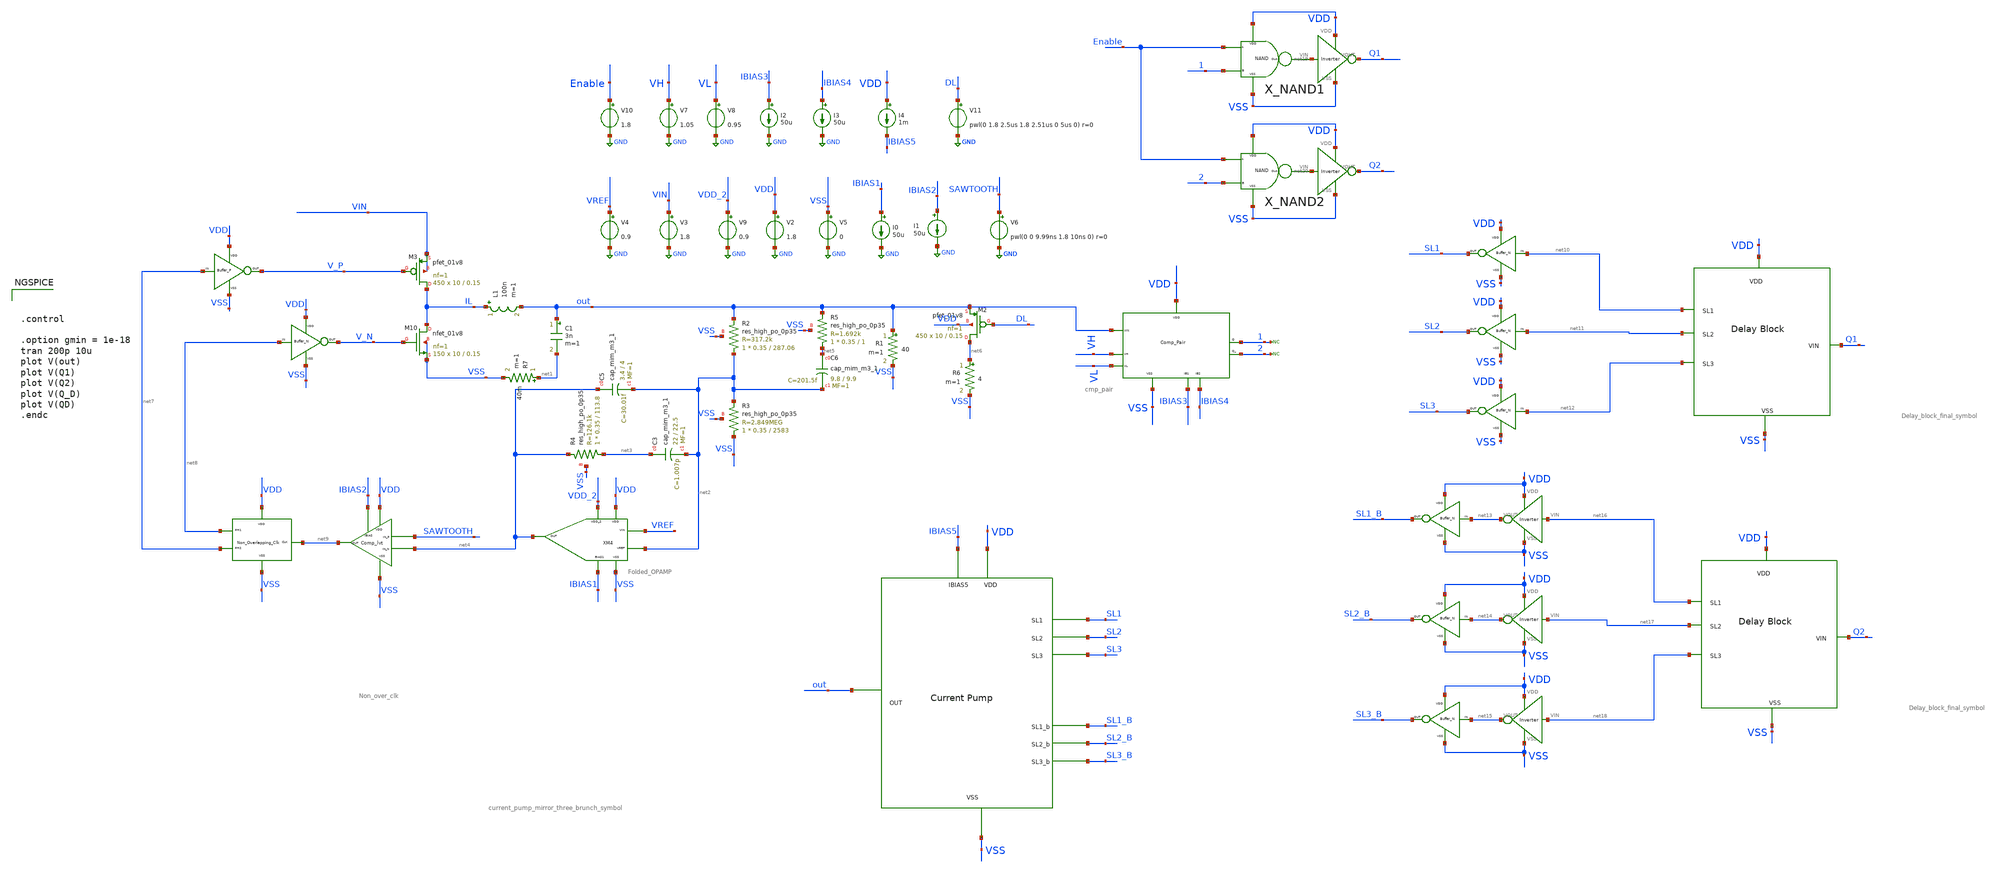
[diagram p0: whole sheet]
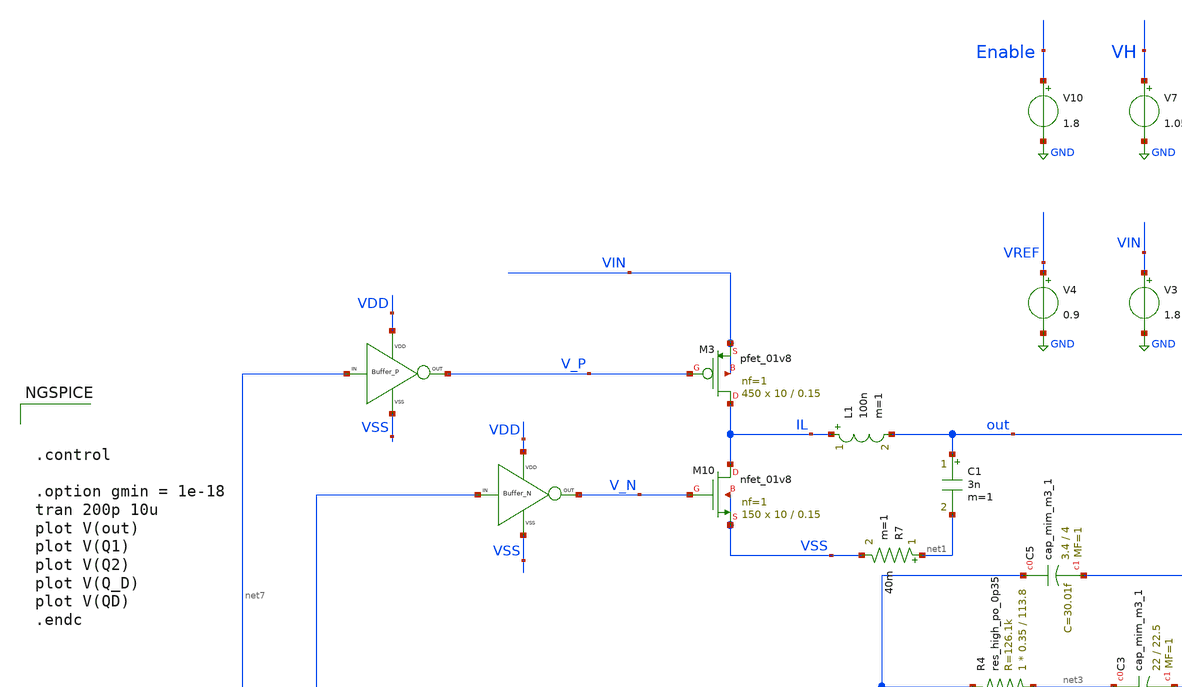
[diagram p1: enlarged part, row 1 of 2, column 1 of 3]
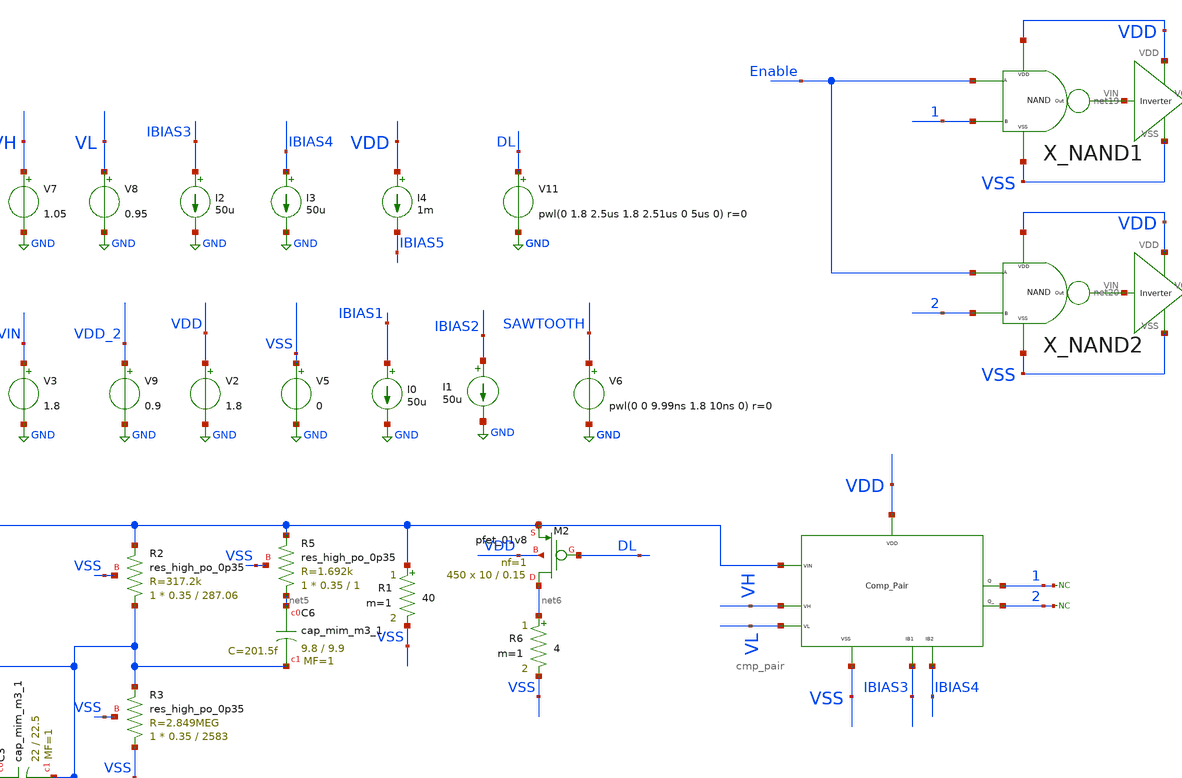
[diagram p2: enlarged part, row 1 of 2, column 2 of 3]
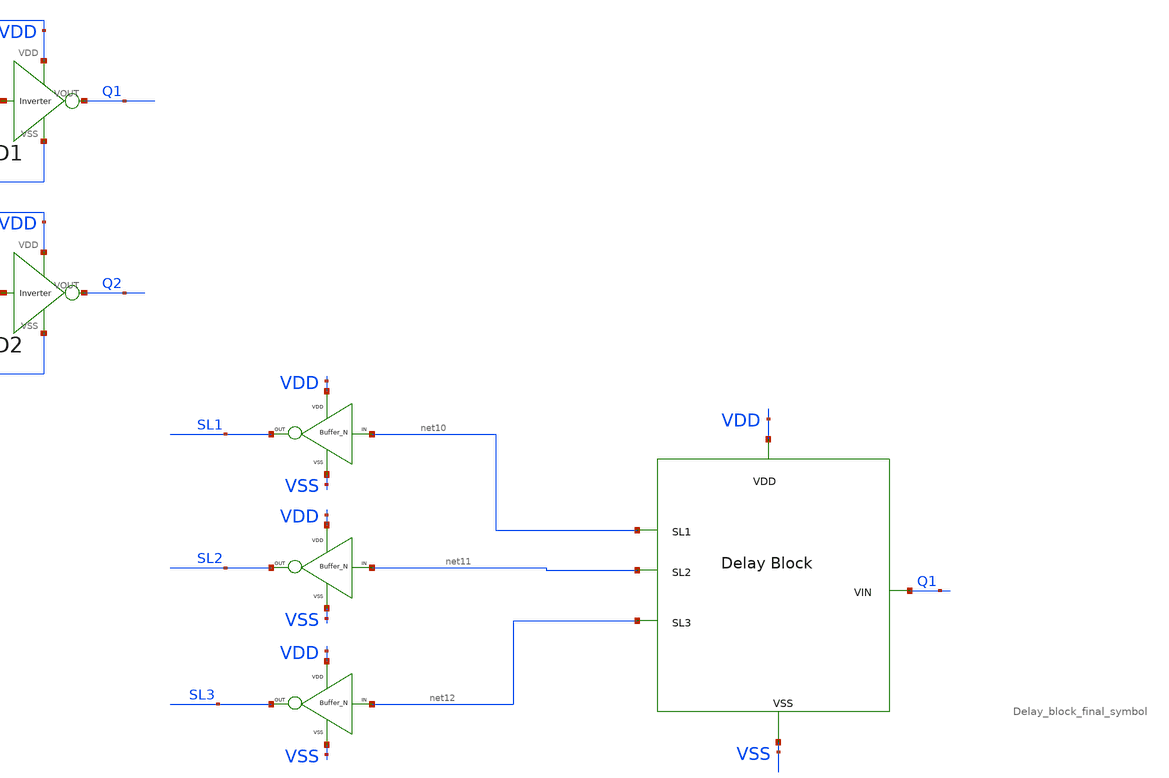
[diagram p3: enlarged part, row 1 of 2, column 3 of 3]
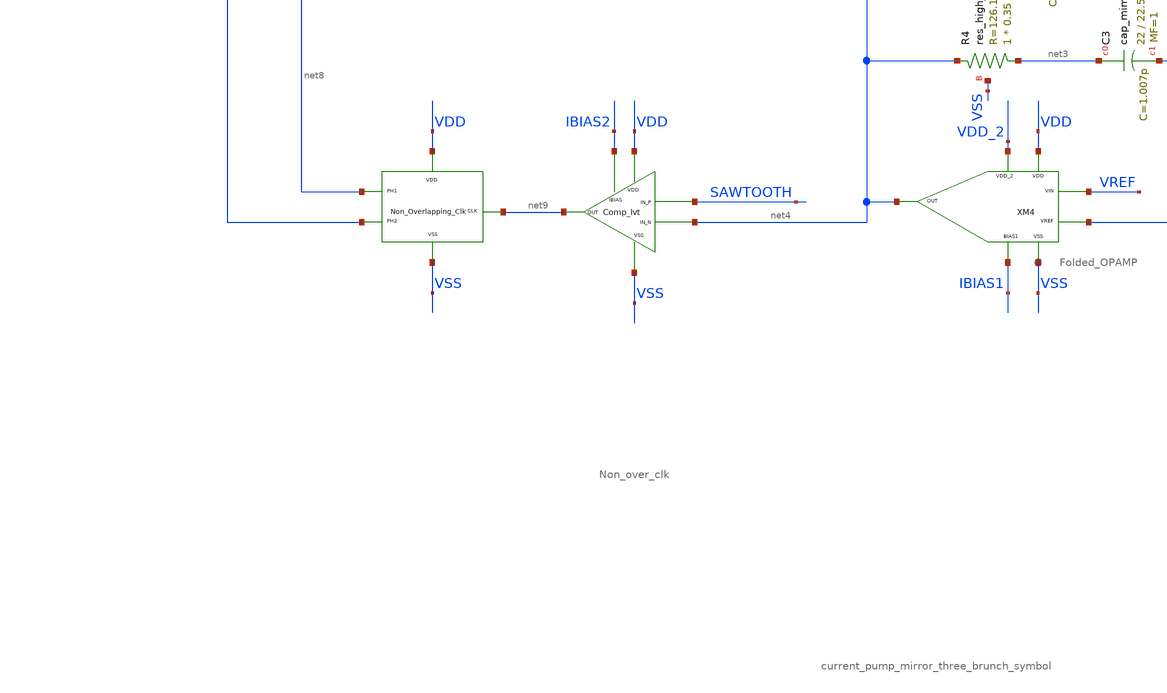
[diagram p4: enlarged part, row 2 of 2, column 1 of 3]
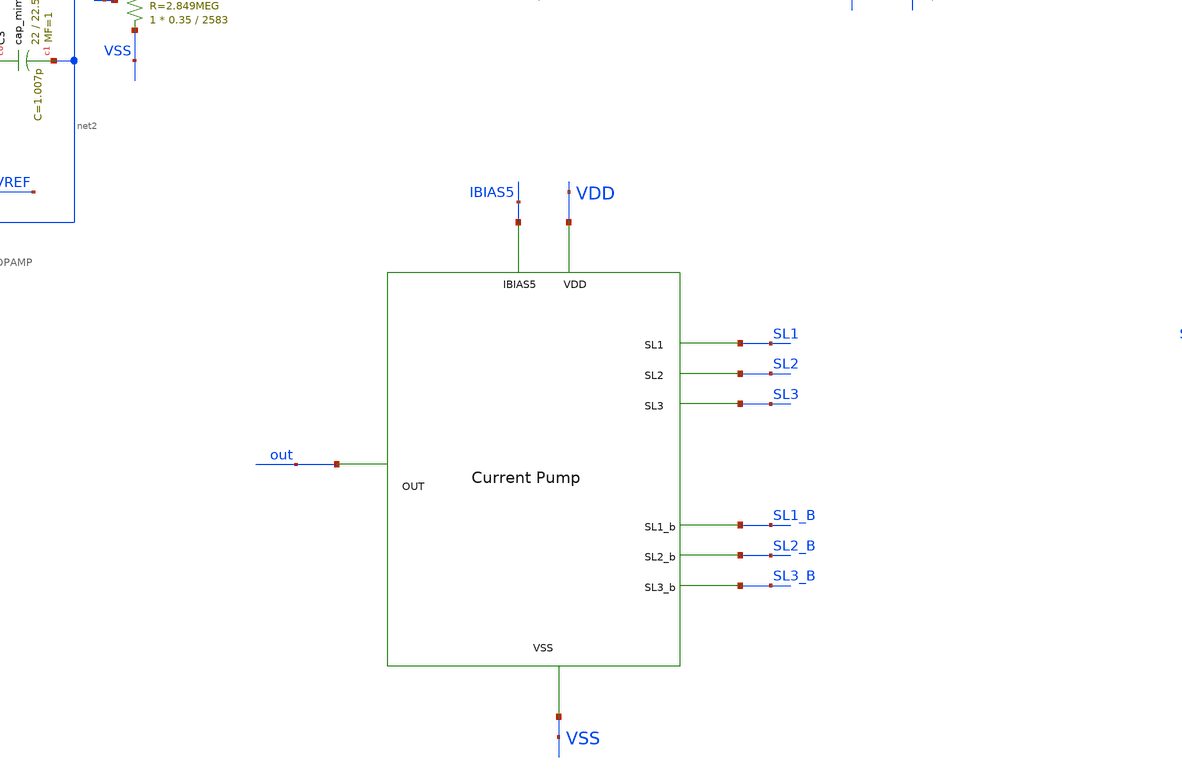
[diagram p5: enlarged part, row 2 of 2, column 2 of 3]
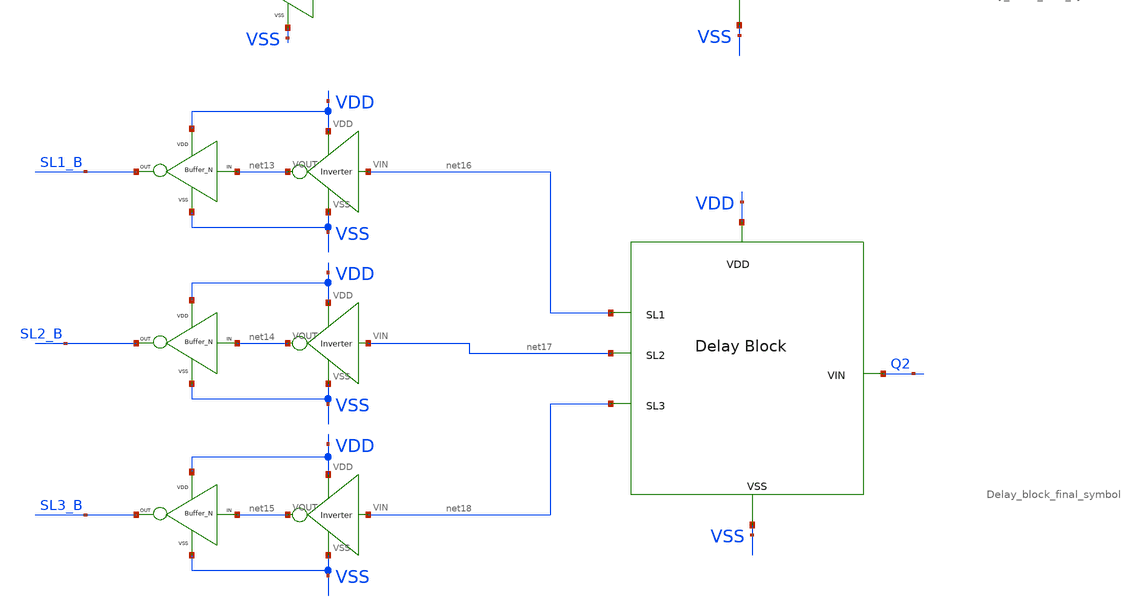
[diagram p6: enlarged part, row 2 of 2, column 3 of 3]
** sch_path: xschem/DC_DC_Converter_xschem/OTHERS/DC_DC_Converter_JV10/TOP_LEVEL/closed_loop_jd_sep_v2.sch
**.subckt closed_loop_jd_sep_v2
XM3 IL V_P VIN VIN sky130_fd_pr__pfet_01v8 L=0.15 W=10 nf=1 ad='int((nf+1)/2) * W/nf * 0.29' as='int((nf+2)/2) * W/nf * 0.29'
+ pd='2*int((nf+1)/2) * (W/nf + 0.29)' ps='2*int((nf+2)/2) * (W/nf + 0.29)' nrd='0.29 / W' nrs='0.29 / W'
+ sa=0 sb=0 sd=0 mult=450 m=450
L1 IL out 100n m=1
C1 out net1 3n m=1
V3 VIN GND 1.8
I0 IBIAS1 GND 50u
V9 VDD_2 GND 0.9
V2 VDD GND 1.8
V5 VSS GND 0
V4 VREF GND 0.9
I1 IBIAS2 GND 50u
V6 SAWTOOTH GND pwl(0 0 9.99ns 1.8 10ns 0) r=0
XM2 net6 DL out VDD sky130_fd_pr__pfet_01v8 L=0.15 W=10 nf=1 ad='int((nf+1)/2) * W/nf * 0.29' as='int((nf+2)/2) * W/nf * 0.29'
+ pd='2*int((nf+1)/2) * (W/nf + 0.29)' ps='2*int((nf+2)/2) * (W/nf + 0.29)' nrd='0.29 / W' nrs='0.29 / W'
+ sa=0 sb=0 sd=0 mult=450 m=450
X101 net7 V_P VDD VSS BUFFER_P
X2 net8 V_N VDD VSS BUFFER_N
XM3 VDD net9 net8 VSS net7 Non_over_clk
XM4 VDD VSS VDD_2 IBIAS1 net4 VREF net2 Folded_OPAMP
XC5 net4 net2 sky130_fd_pr__cap_mim_m3_1 W=3.4 L=4 MF=1 m=1
XC3 net3 net2 sky130_fd_pr__cap_mim_m3_1 W=22 L=22.5 MF=1 m=1
XC6 net5 net2 sky130_fd_pr__cap_mim_m3_1 W=9.8 L=9.9 MF=1 m=1
XM10 IL V_N VSS VSS sky130_fd_pr__nfet_01v8 L=0.15 W=10 nf=1 ad='int((nf+1)/2) * W/nf * 0.29' as='int((nf+2)/2) * W/nf * 0.29'
+ pd='2*int((nf+1)/2) * (W/nf + 0.29)' ps='2*int((nf+2)/2) * (W/nf + 0.29)' nrd='0.29 / W' nrs='0.29 / W'
+ sa=0 sb=0 sd=0 mult=150 m=150
XR4 net3 net4 VSS sky130_fd_pr__res_high_po_0p35 L=113.8 mult=1 m=1
XR5 net5 out VSS sky130_fd_pr__res_high_po_0p35 L=1 mult=1 m=1
XR2 net2 out VSS sky130_fd_pr__res_high_po_0p35 L=287.06 mult=1 m=1
XR3 VSS net2 VSS sky130_fd_pr__res_high_po_0p35 L=2583 mult=1 m=1
R7 net1 VSS 40m m=1
R1 out VSS 40 m=1
R6 net6 VSS 4 m=1
XM2 IBIAS2 VDD SAWTOOTH net4 VSS net9 Comp_lvt
XM1 VDD VSS out VH VL IBIAS3 IBIAS4 1 2 cmp_pair
V7 VH GND 1.05
V8 VL GND 0.95
I2 IBIAS3 GND 50u
I3 IBIAS4 GND 50u
* noconn 2
* noconn 1
X_NAND1 VDD VSS Enable 1 net19 NAND
X_NAND2 VDD VSS Enable 2 net20 NAND
X9 VSS VDD net19 Q1 Inverter
X10 VSS VDD net20 Q2 Inverter
V10 Enable GND 1.8
V11 DL GND pwl(0 1.8 2.5us 1.8 2.51us 0 5us 0) r=0
x1 net11 net12 VDD Q1 VSS net10 Delay_block_final_symbol
x2 net17 net18 VDD Q2 VSS net16 Delay_block_final_symbol
X3 VSS VDD net16 net13 Inverter
X4 VSS VDD net17 net14 Inverter
X5 VSS VDD net18 net15 Inverter
x3 VDD IBIAS5 SL3 out SL2 SL1 VSS SL3_B SL2_B SL1_B current_pump_mirror_three_brunch_symbol
I4 VDD IBIAS5 1m
X6 net14 SL2_B VDD VSS BUFFER_N
X7 net15 SL3_B VDD VSS BUFFER_N
X8 net13 SL1_B VDD VSS BUFFER_N
X11 net11 SL2 VDD VSS BUFFER_N
X12 net12 SL3 VDD VSS BUFFER_N
X13 net10 SL1 VDD VSS BUFFER_N
**** begin user architecture code

** opencircuitdesign pdks install
.lib $::SKYWATER_MODELS/sky130.lib.spice tt





.control

.option gmin = 1e-18
tran 200p 10u
plot V(out)
plot V(Q1)
plot V(Q2)
plot V(Q_D)
plot V(QD)
.endc


**** end user architecture code
**.ends
.GLOBAL GND
.end
